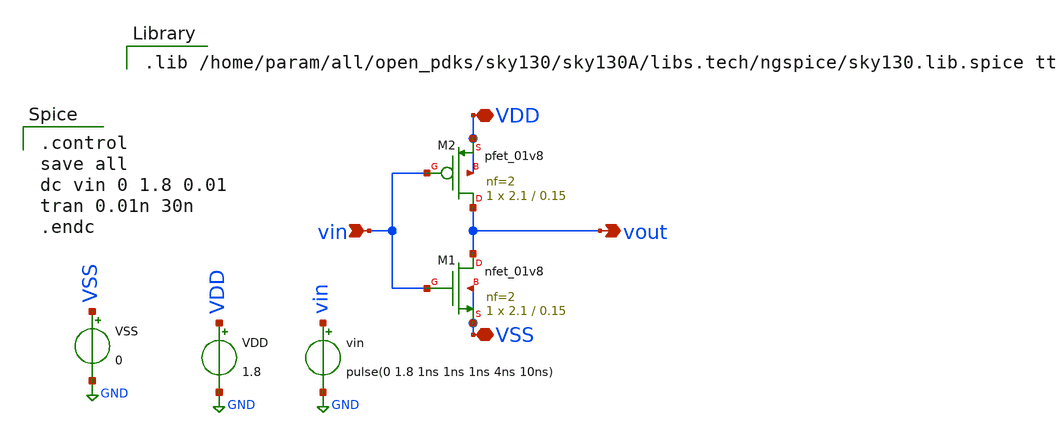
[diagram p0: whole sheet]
** sch_path: invertor_test.sch
**.subckt invertor_test VDD VSS vin vout
*.iopin VDD
*.iopin VSS
*.ipin vin
*.opin vout
XM1 vout vin VSS VSS sky130_fd_pr__nfet_01v8 L=0.15 W=2.1 nf=2 ad='int((nf+1)/2) * W/nf * 0.29' as='int((nf+2)/2) * W/nf * 0.29'
+ pd='2*int((nf+1)/2) * (W/nf + 0.29)' ps='2*int((nf+2)/2) * (W/nf + 0.29)' nrd='0.29 / W' nrs='0.29 / W'
+ sa=0 sb=0 sd=0 mult=1 m=1
XM2 vout vin VDD VDD sky130_fd_pr__pfet_01v8 L=0.15 W=2.1 nf=2 ad='int((nf+1)/2) * W/nf * 0.29' as='int((nf+2)/2) * W/nf * 0.29'
+ pd='2*int((nf+1)/2) * (W/nf + 0.29)' ps='2*int((nf+2)/2) * (W/nf + 0.29)' nrd='0.29 / W' nrs='0.29 / W'
+ sa=0 sb=0 sd=0 mult=1 m=1
vin vin GND pulse(0 1.8 1ns 1ns 1ns 4ns 10ns)
VDD VDD GND 1.8
VSS VSS GND 0
**** begin user architecture code

.control
save all
dc vin 0 1.8 0.01
tran 0.01n 30n
.endc


.lib /home/param/all/open_pdks/sky130/sky130A/libs.tech/ngspice/sky130.lib.spice tt

**** end user architecture code
**.ends
.GLOBAL GND
.end
